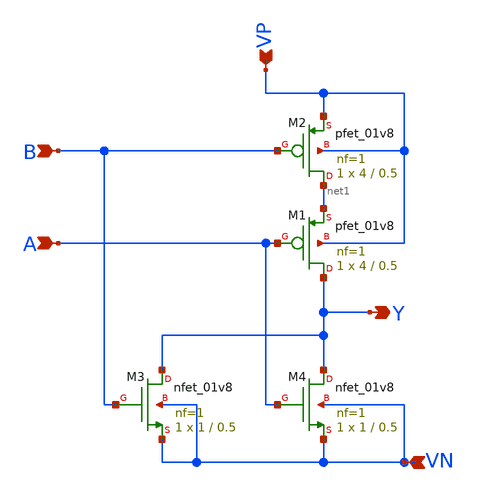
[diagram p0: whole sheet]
** sch_path: ADC/4bit_C2C/MagicAndSpice/EE431_FinalProj/NOR2.sch
**.subckt NOR2 A B VP VN Y
*.ipin A
*.ipin B
*.ipin VP
*.ipin VN
*.opin Y
XM1 Y A net1 VP sky130_fd_pr__pfet_01v8 L=0.5 W=4 nf=1 ad='int((nf+1)/2) * W/nf * 0.29' as='int((nf+2)/2) * W/nf * 0.29'
+ pd='2*int((nf+1)/2) * (W/nf + 0.29)' ps='2*int((nf+2)/2) * (W/nf + 0.29)' nrd='0.29 / W' nrs='0.29 / W'
+ sa=0 sb=0 sd=0 mult=1 m=1
XM2 net1 B VP VP sky130_fd_pr__pfet_01v8 L=0.5 W=4 nf=1 ad='int((nf+1)/2) * W/nf * 0.29' as='int((nf+2)/2) * W/nf * 0.29'
+ pd='2*int((nf+1)/2) * (W/nf + 0.29)' ps='2*int((nf+2)/2) * (W/nf + 0.29)' nrd='0.29 / W' nrs='0.29 / W'
+ sa=0 sb=0 sd=0 mult=1 m=1
XM3 Y B VN VN sky130_fd_pr__nfet_01v8 L=0.5 W=1 nf=1 ad='int((nf+1)/2) * W/nf * 0.29' as='int((nf+2)/2) * W/nf * 0.29'
+ pd='2*int((nf+1)/2) * (W/nf + 0.29)' ps='2*int((nf+2)/2) * (W/nf + 0.29)' nrd='0.29 / W' nrs='0.29 / W'
+ sa=0 sb=0 sd=0 mult=1 m=1
XM4 Y A VN VN sky130_fd_pr__nfet_01v8 L=0.5 W=1 nf=1 ad='int((nf+1)/2) * W/nf * 0.29' as='int((nf+2)/2) * W/nf * 0.29'
+ pd='2*int((nf+1)/2) * (W/nf + 0.29)' ps='2*int((nf+2)/2) * (W/nf + 0.29)' nrd='0.29 / W' nrs='0.29 / W'
+ sa=0 sb=0 sd=0 mult=1 m=1
**.ends
.end
